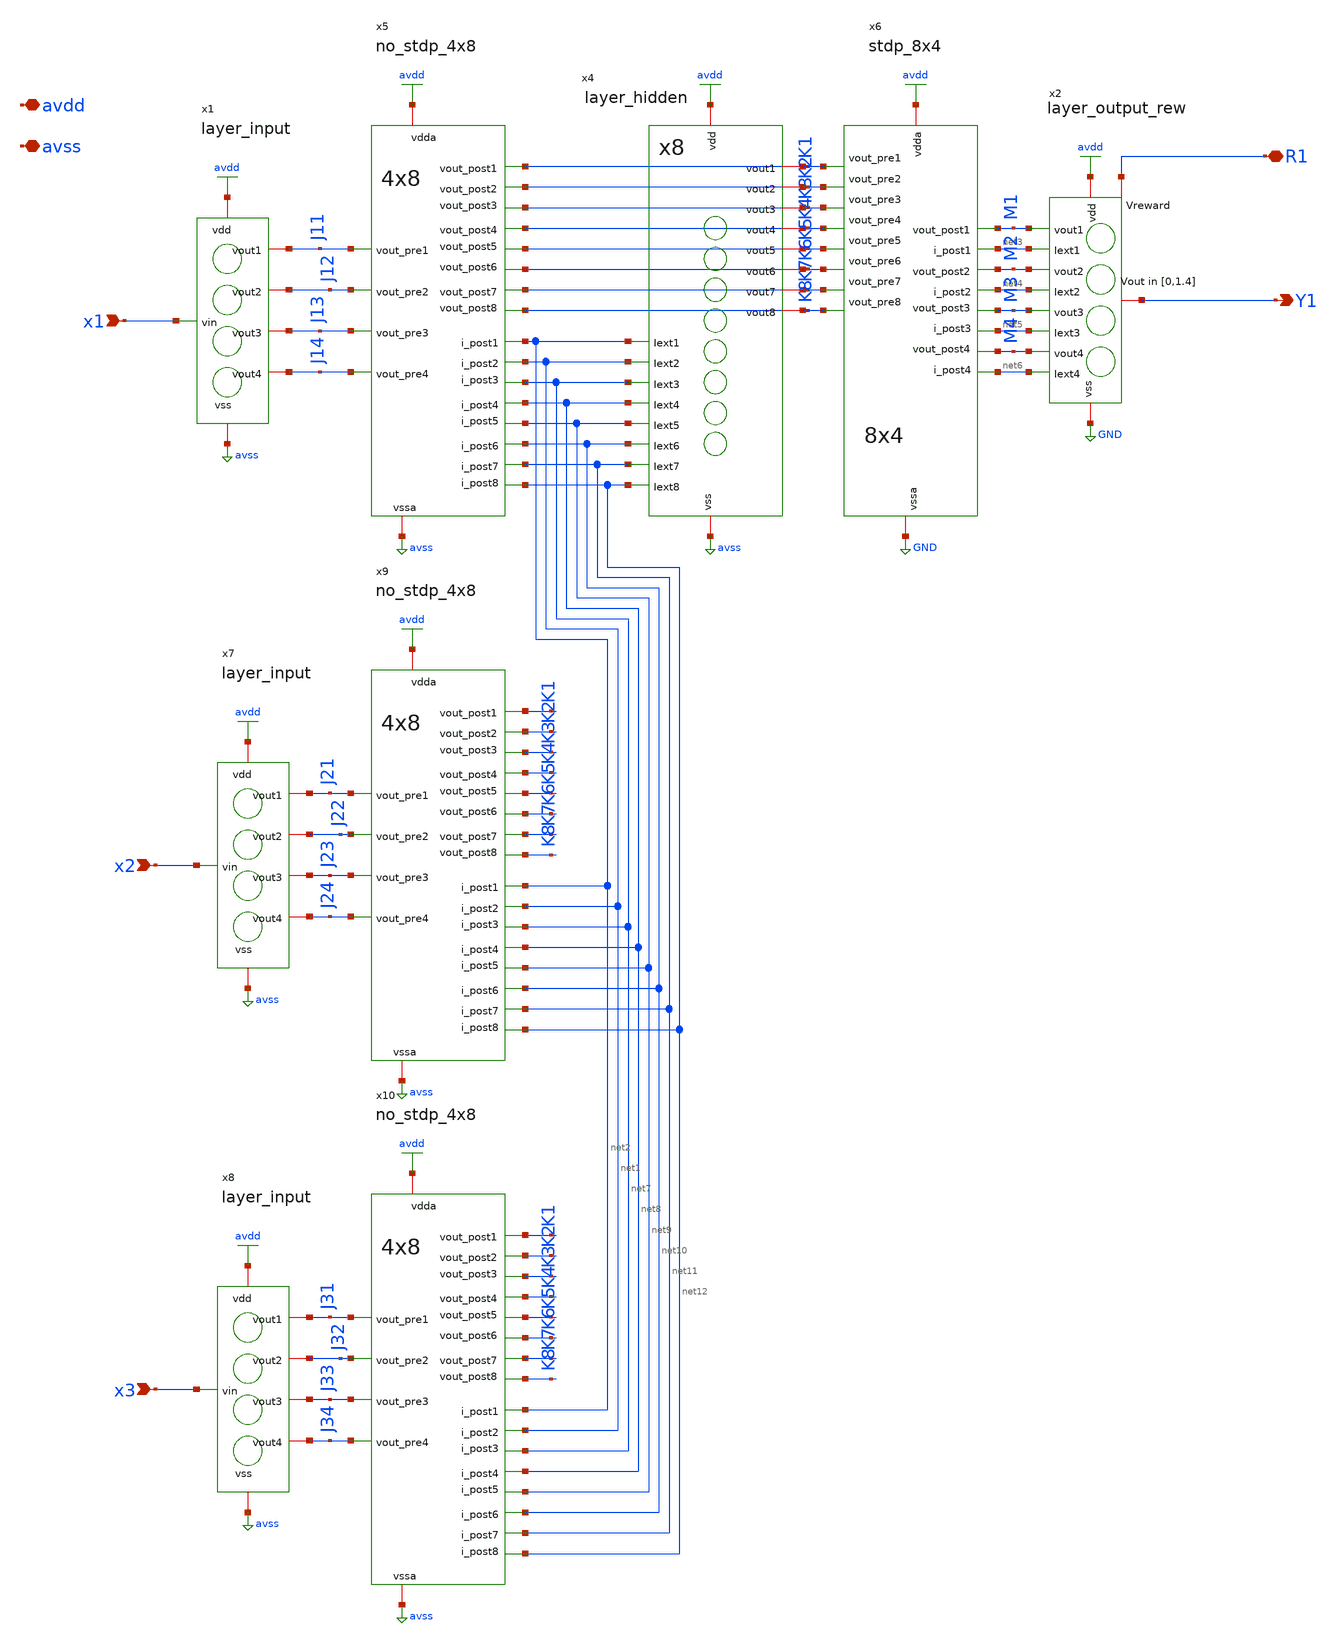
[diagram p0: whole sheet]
** sch_path: 3x1_net.sch
**.subckt 3x1_net x1 x3 x2 avdd avss Y1 R1
*.ipin x1
*.ipin x3
*.ipin x2
*.iopin avdd
*.iopin avss
*.opin Y1
*.iopin R1
x1 avdd avss x1 J11 J12 J13 J14 layer_input
x4 avdd net2 avss net1 net7 K1 K2 net8 K3 net9 K4 net10 K5 net11 K6 K7 net12 K8 layer_hidden
x5 avdd net2 net1 net7 avss K1 K2 net11 net12 net9 K3 net8 net10 K8 K7 K6 K5 K4 J11 J12 J13 J14
+ no_stdp_4x8
x6 net4 net3 M2 net5 GND M1 M3 net6 M4 K1 K2 K3 K4 K5 K6 K7 K8 avdd stdp_8x4
x2 avdd net3 GND net4 net5 Y1 net6 M1 M2 M3 M4 R1 layer_output_rew
x7 avdd avss x2 J21 J22 J23 J24 layer_input
x8 avdd avss x3 J31 J32 J33 J34 layer_input
x9 avdd net2 net1 net7 avss K1 K2 net11 net12 net9 K3 net8 net10 K8 K7 K6 K5 K4 J21 J22 J23 J24
+ no_stdp_4x8
x10 avdd net2 net1 net7 avss K1 K2 net11 net12 net9 K3 net8 net10 K8 K7 K6 K5 K4 J31 J32 J33 J34
+ no_stdp_4x8
**.ends
.GLOBAL avss
.GLOBAL avdd
.GLOBAL GND
.end
